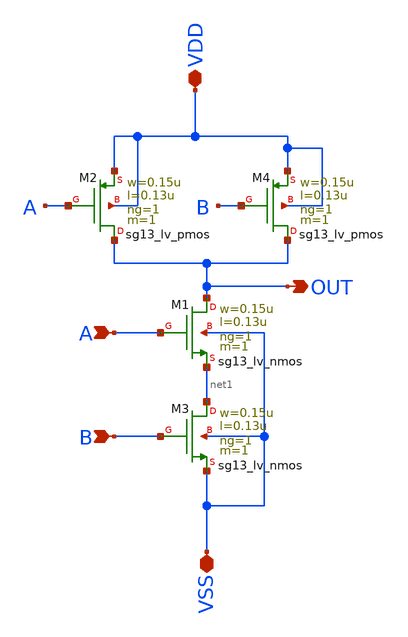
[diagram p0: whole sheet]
** sch_path: CDR4176-main/schematic/xschem/nand_custom/nand_custom.sch
**.subckt nand_custom VDD VSS A B OUT
*.iopin VDD
*.iopin VSS
*.ipin A
*.ipin B
*.opin OUT
XM1 OUT A net1 VSS sg13_lv_nmos w=0.15u l=0.13u ng=1 m=1 mm_ok=1
XM2 OUT A VDD VDD sg13_lv_pmos w=0.15u l=0.13u ng=1 m=1 mm_ok=1
XM3 net1 B VSS VSS sg13_lv_nmos w=0.15u l=0.13u ng=1 m=1 mm_ok=1
XM4 OUT B VDD VDD sg13_lv_pmos w=0.15u l=0.13u ng=1 m=1 mm_ok=1
**.ends
.end
